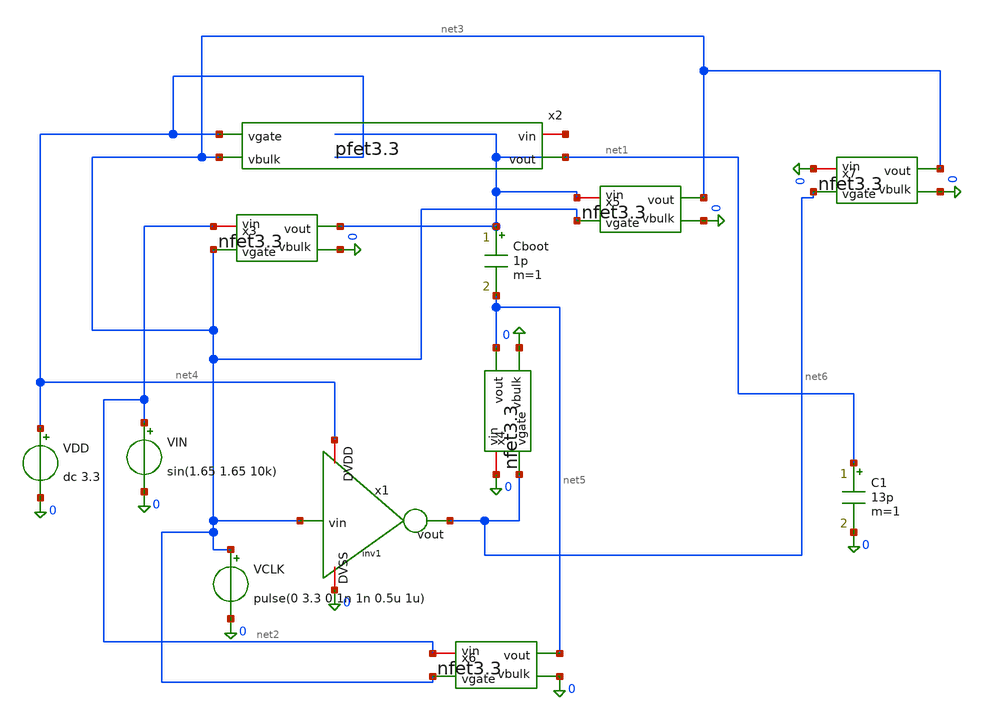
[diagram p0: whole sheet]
** sch_path: designs/emily_testing/TB_swtich2.sch
**.subckt TB_swtich2
VCLK net3 0 pulse(0 3.3 0 1n 1n 0.5u 1u)
VIN net2 0 sin(1.65 1.65 10k)
C1 net1 0 13p m=1
x2 net7 net4 net3 net1 pfet3.3
x3 net1 net3 0 net2 nfet3.3
x4 net5 net6 0 0 nfet3.3
x5 net3 net3 0 net1 nfet3.3
x6 net5 net3 0 net2 nfet3.3
x7 net3 net6 0 0 nfet3.3
VDD net4 0 dc 3.3
x1 net4 net3 net6 0 inv1
Cboot net1 net5 1p m=1
**** begin user architecture code


.param c_area=0
.param mc_c_cox_1p0fF=0 mc_c_cox_1p5fF=0 mc_c_cox_2p0fF=0
.lib /foss/pdks/gf180mcuD/libs.tech/ngspice/sm141064.ngspice typical
.lib /foss/pdks/gf180mcuD/libs.tech/ngspice/sm141064_mim.ngspice cap_mim_new
.include /foss/pdks/gf180mcuD/libs.tech/ngspice/design.ngspice
.param var_vth=0 var_k=0
.options savecurrents
.control
  save all
  tran 2n 3u
  let vin = v(net2)
  let clk = v(net3)
  let vout = v(net1)
  plot clk vin vout
.endc



**** end user architecture code
**.ends

* expanding   symbol:  designs/emily_testing/pfet3.3.sym # of pins=4
** sym_path: designs/emily_testing/pfet3.3.sym
** sch_path: designs/emily_testing/pfet3.3.sch
.subckt pfet3.3 vin vgate vbulk vout
*.opin vout
*.ipin vgate
*.iopin vin
*.ipin vbulk
XM1 vout vgate vin vbulk pfet_03v3 L=0.28u W=0.22u nf=1 ad='int((nf+1)/2) * W/nf * 0.18u' as='int((nf+2)/2) * W/nf * 0.18u'
+ pd='2*int((nf+1)/2) * (W/nf + 0.18u)' ps='2*int((nf+2)/2) * (W/nf + 0.18u)' nrd='0.18u / W' nrs='0.18u / W'
+ sa=0 sb=0 sd=0 m=1
.ends


* expanding   symbol:  designs/emily_testing/nfet3.3.sym # of pins=4
** sym_path: designs/emily_testing/nfet3.3.sym
** sch_path: designs/emily_testing/nfet3.3.sch
.subckt nfet3.3 vout vgate vbulk vin
*.opin vout
*.ipin vgate
*.iopin vin
*.ipin vbulk
XM1 vout vgate vin vbulk nfet_03v3 L=0.28u W=0.22u nf=1 ad='int((nf+1)/2) * W/nf * 0.18u' as='int((nf+2)/2) * W/nf * 0.18u'
+ pd='2*int((nf+1)/2) * (W/nf + 0.18u)' ps='2*int((nf+2)/2) * (W/nf + 0.18u)' nrd='0.18u / W' nrs='0.18u / W'
+ sa=0 sb=0 sd=0 m=1
.ends


* expanding   symbol:  designs/emily_testing/inv1.sym # of pins=4
** sym_path: sar_logic/sar_designs/inv1.sym
** sch_path: sar_logic/sar_designs/inv1.sch
.subckt inv1 DVDD vin vout DVSS
*.ipin vin
*.opin vout
*.iopin DVDD
*.iopin DVSS
XM1 vout vin DVDD DVDD pfet_03v3 L=0.3u W=1.7u nf=1 ad='int((nf+1)/2) * W/nf * 0.18u' as='int((nf+2)/2) * W/nf * 0.18u'
+ pd='2*int((nf+1)/2) * (W/nf + 0.18u)' ps='2*int((nf+2)/2) * (W/nf + 0.18u)' nrd='0.18u / W' nrs='0.18u / W'
+ sa=0 sb=0 sd=0 m=1
XM2 vout vin DVSS DVSS nfet_03v3 L=0.3u W=0.85u nf=1 ad='int((nf+1)/2) * W/nf * 0.18u' as='int((nf+2)/2) * W/nf * 0.18u'
+ pd='2*int((nf+1)/2) * (W/nf + 0.18u)' ps='2*int((nf+2)/2) * (W/nf + 0.18u)' nrd='0.18u / W' nrs='0.18u / W'
+ sa=0 sb=0 sd=0 m=1
.ends

.end
